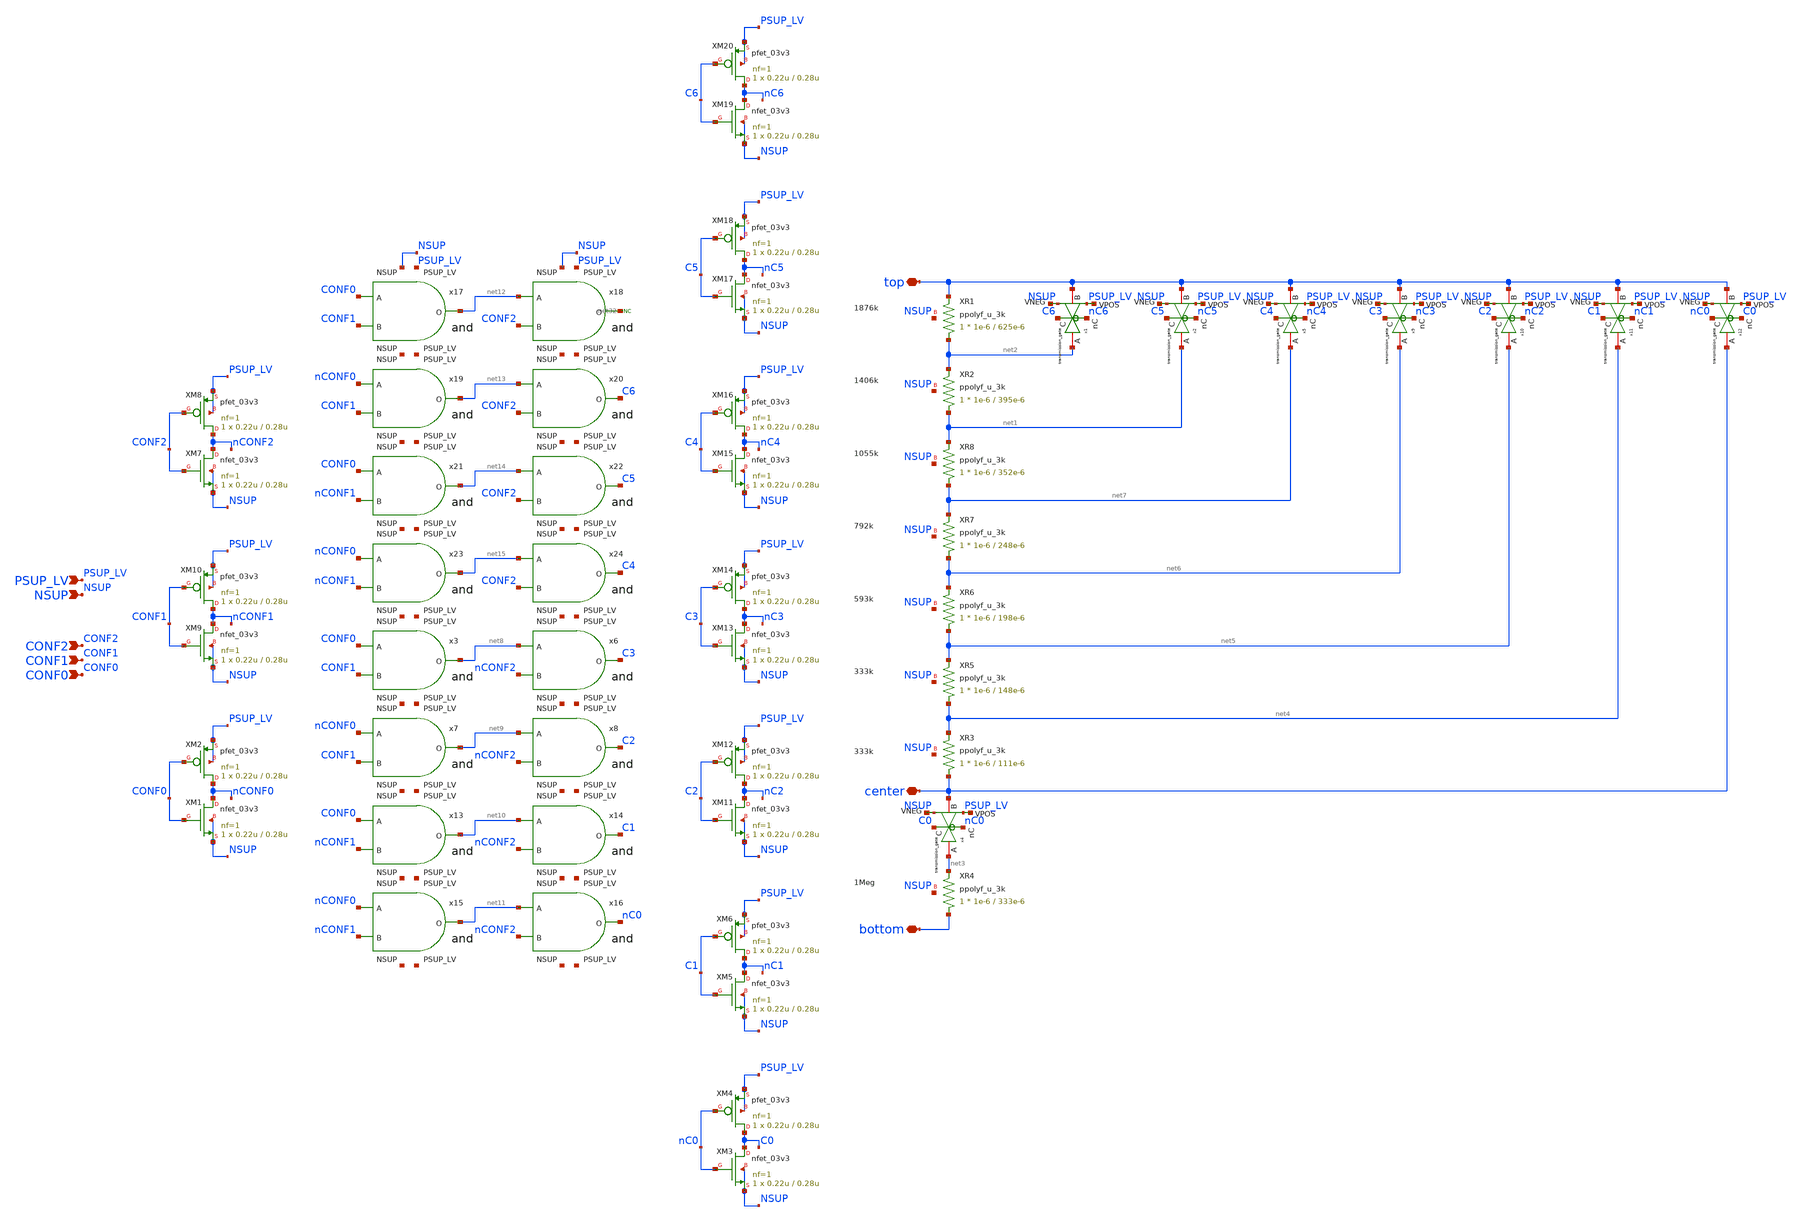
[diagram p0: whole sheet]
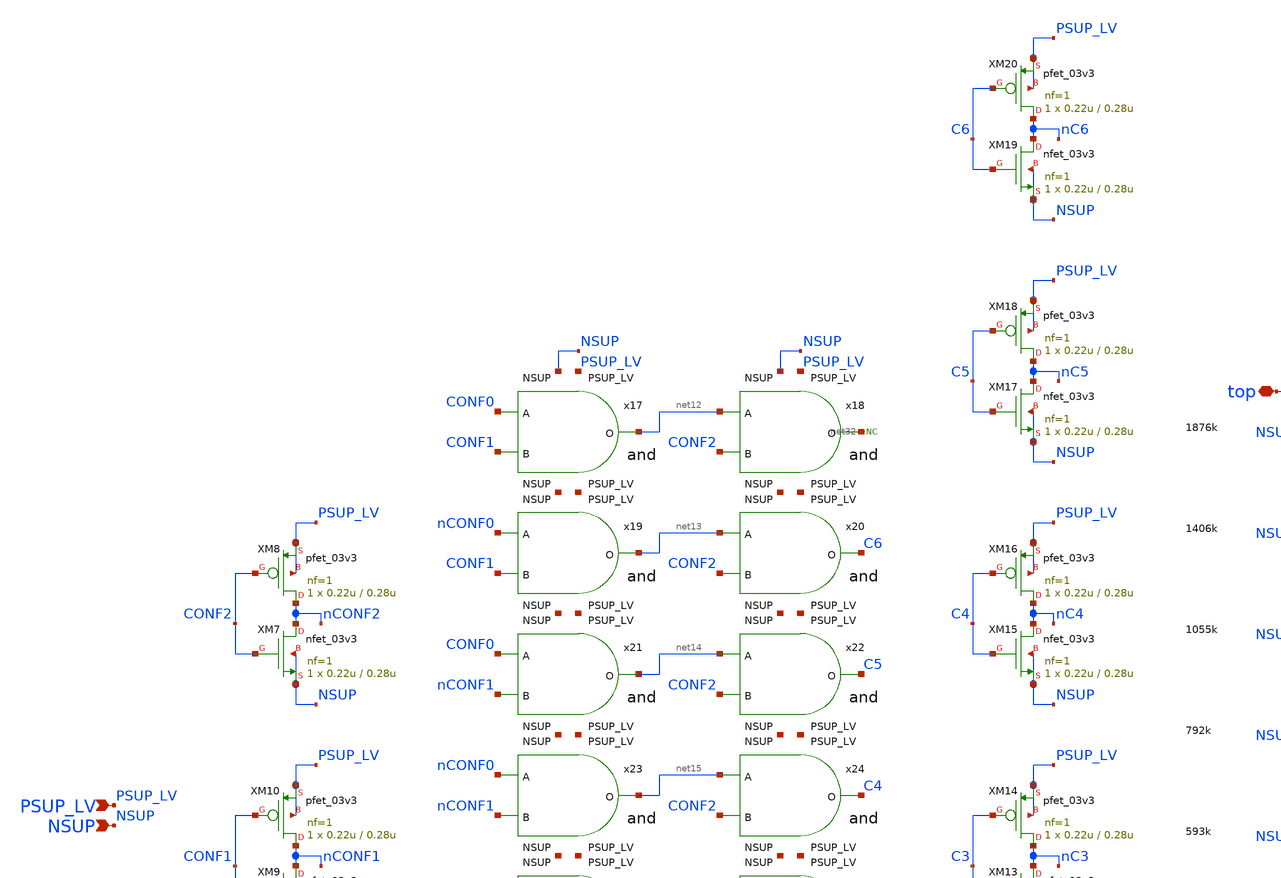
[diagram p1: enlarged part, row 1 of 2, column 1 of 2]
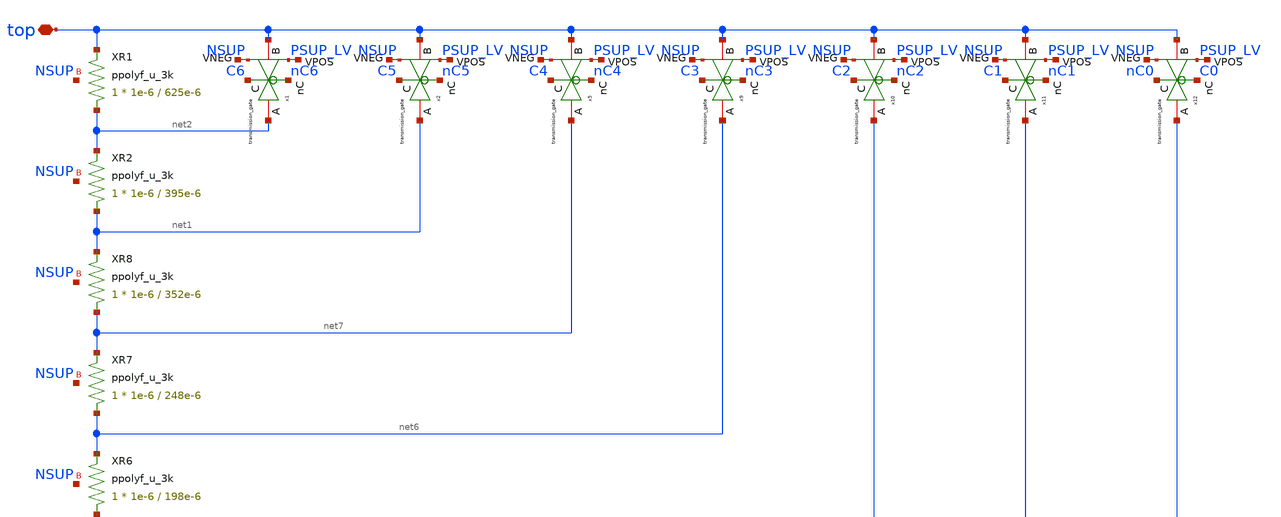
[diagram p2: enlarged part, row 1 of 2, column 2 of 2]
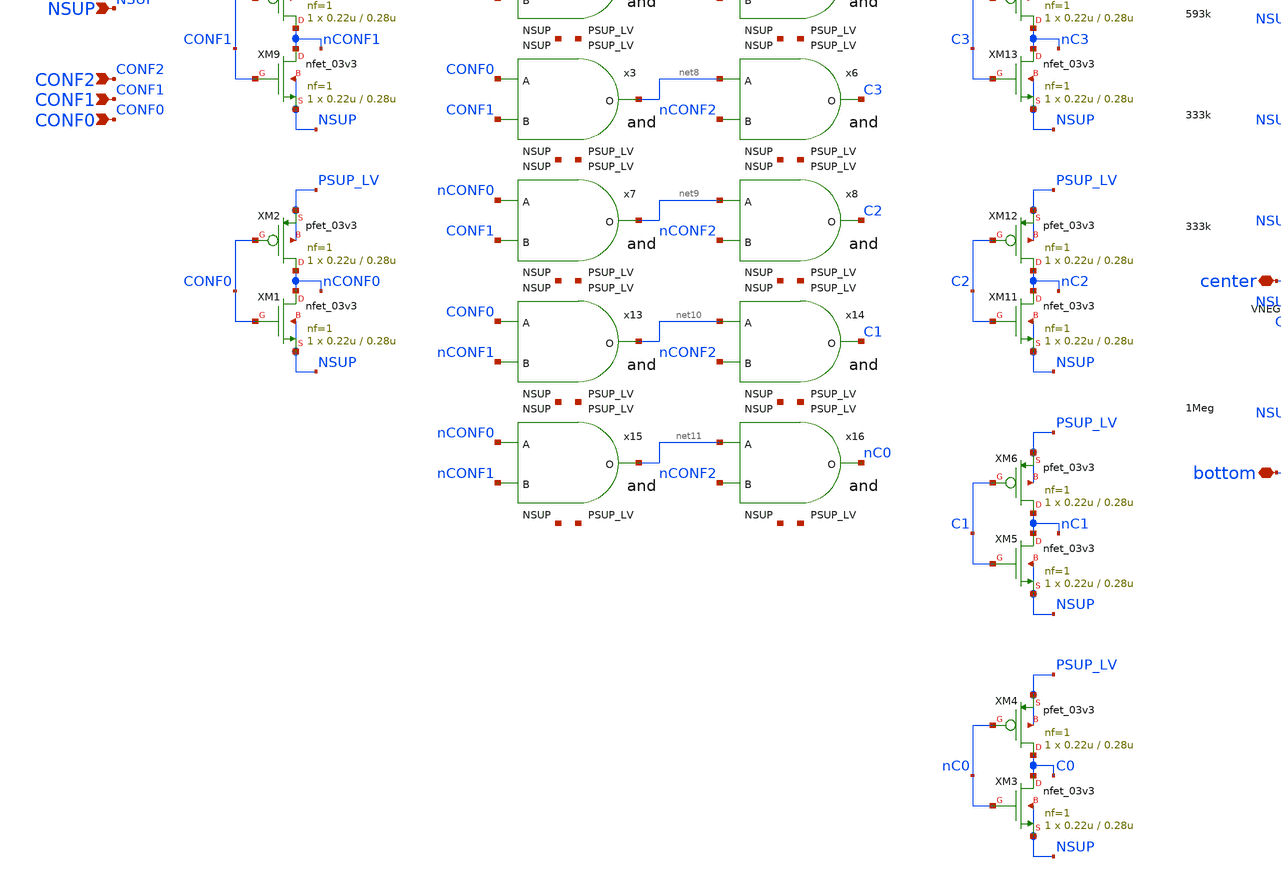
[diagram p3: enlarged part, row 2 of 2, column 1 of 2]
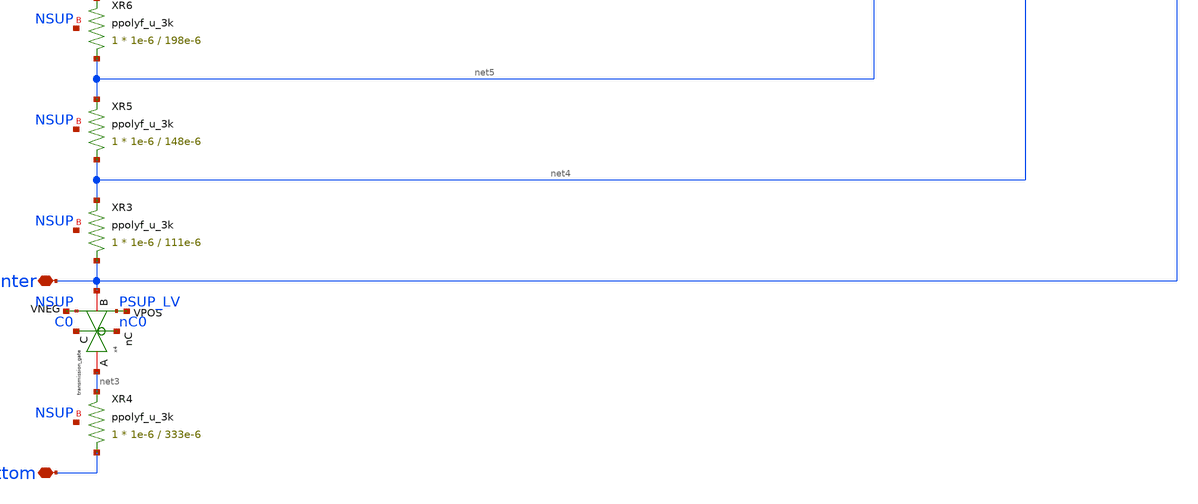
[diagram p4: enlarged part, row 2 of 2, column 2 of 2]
** sch_path: xschem/blocks/LPF_gain_fb/LPF_gain_fb.sch
**.subckt LPF_gain_fb top center bottom PSUP_LV NSUP CONF1 CONF2 CONF0
*.iopin top
*.iopin center
*.iopin bottom
*.ipin PSUP_LV
*.ipin NSUP
*.ipin CONF1
*.ipin CONF2
*.ipin CONF0
XR1 net2 top NSUP ppolyf_u_3k r_width=1e-6 r_length=625e-6 m=1
XR2 net1 net2 NSUP ppolyf_u_3k r_width=1e-6 r_length=395e-6 m=1
XR3 center net4 NSUP ppolyf_u_3k r_width=1e-6 r_length=111e-6 m=1
XR4 bottom net3 NSUP ppolyf_u_3k r_width=1e-6 r_length=333e-6 m=1
XM7 nCONF2 CONF2 NSUP NSUP nfet_03v3 L=0.28u W=0.22u nf=1 ad='int((nf+1)/2) * W/nf * 0.18u' as='int((nf+2)/2) * W/nf * 0.18u'
+ pd='2*int((nf+1)/2) * (W/nf + 0.18u)' ps='2*int((nf+2)/2) * (W/nf + 0.18u)' nrd='0.18u / W' nrs='0.18u / W'
+ sa=0 sb=0 sd=0 m=1
XM8 nCONF2 CONF2 PSUP_LV PSUP_LV pfet_03v3 L=0.28u W=0.22u nf=1 ad='int((nf+1)/2) * W/nf * 0.18u' as='int((nf+2)/2) * W/nf * 0.18u'
+ pd='2*int((nf+1)/2) * (W/nf + 0.18u)' ps='2*int((nf+2)/2) * (W/nf + 0.18u)' nrd='0.18u / W' nrs='0.18u / W'
+ sa=0 sb=0 sd=0 m=1
XM9 nCONF1 CONF1 NSUP NSUP nfet_03v3 L=0.28u W=0.22u nf=1 ad='int((nf+1)/2) * W/nf * 0.18u' as='int((nf+2)/2) * W/nf * 0.18u'
+ pd='2*int((nf+1)/2) * (W/nf + 0.18u)' ps='2*int((nf+2)/2) * (W/nf + 0.18u)' nrd='0.18u / W' nrs='0.18u / W'
+ sa=0 sb=0 sd=0 m=1
XM10 nCONF1 CONF1 PSUP_LV PSUP_LV pfet_03v3 L=0.28u W=0.22u nf=1 ad='int((nf+1)/2) * W/nf * 0.18u' as='int((nf+2)/2) * W/nf * 0.18u'
+ pd='2*int((nf+1)/2) * (W/nf + 0.18u)' ps='2*int((nf+2)/2) * (W/nf + 0.18u)' nrd='0.18u / W' nrs='0.18u / W'
+ sa=0 sb=0 sd=0 m=1
XM1 nCONF0 CONF0 NSUP NSUP nfet_03v3 L=0.28u W=0.22u nf=1 ad='int((nf+1)/2) * W/nf * 0.18u' as='int((nf+2)/2) * W/nf * 0.18u'
+ pd='2*int((nf+1)/2) * (W/nf + 0.18u)' ps='2*int((nf+2)/2) * (W/nf + 0.18u)' nrd='0.18u / W' nrs='0.18u / W'
+ sa=0 sb=0 sd=0 m=1
XM2 nCONF0 CONF0 PSUP_LV PSUP_LV pfet_03v3 L=0.28u W=0.22u nf=1 ad='int((nf+1)/2) * W/nf * 0.18u' as='int((nf+2)/2) * W/nf * 0.18u'
+ pd='2*int((nf+1)/2) * (W/nf + 0.18u)' ps='2*int((nf+2)/2) * (W/nf + 0.18u)' nrd='0.18u / W' nrs='0.18u / W'
+ sa=0 sb=0 sd=0 m=1
XM3 C0 nC0 NSUP NSUP nfet_03v3 L=0.28u W=0.22u nf=1 ad='int((nf+1)/2) * W/nf * 0.18u' as='int((nf+2)/2) * W/nf * 0.18u'
+ pd='2*int((nf+1)/2) * (W/nf + 0.18u)' ps='2*int((nf+2)/2) * (W/nf + 0.18u)' nrd='0.18u / W' nrs='0.18u / W'
+ sa=0 sb=0 sd=0 m=1
XM4 C0 nC0 PSUP_LV PSUP_LV pfet_03v3 L=0.28u W=0.22u nf=1 ad='int((nf+1)/2) * W/nf * 0.18u' as='int((nf+2)/2) * W/nf * 0.18u'
+ pd='2*int((nf+1)/2) * (W/nf + 0.18u)' ps='2*int((nf+2)/2) * (W/nf + 0.18u)' nrd='0.18u / W' nrs='0.18u / W'
+ sa=0 sb=0 sd=0 m=1
XM5 nC1 C1 NSUP NSUP nfet_03v3 L=0.28u W=0.22u nf=1 ad='int((nf+1)/2) * W/nf * 0.18u' as='int((nf+2)/2) * W/nf * 0.18u'
+ pd='2*int((nf+1)/2) * (W/nf + 0.18u)' ps='2*int((nf+2)/2) * (W/nf + 0.18u)' nrd='0.18u / W' nrs='0.18u / W'
+ sa=0 sb=0 sd=0 m=1
XM6 nC1 C1 PSUP_LV PSUP_LV pfet_03v3 L=0.28u W=0.22u nf=1 ad='int((nf+1)/2) * W/nf * 0.18u' as='int((nf+2)/2) * W/nf * 0.18u'
+ pd='2*int((nf+1)/2) * (W/nf + 0.18u)' ps='2*int((nf+2)/2) * (W/nf + 0.18u)' nrd='0.18u / W' nrs='0.18u / W'
+ sa=0 sb=0 sd=0 m=1
XM11 nC2 C2 NSUP NSUP nfet_03v3 L=0.28u W=0.22u nf=1 ad='int((nf+1)/2) * W/nf * 0.18u' as='int((nf+2)/2) * W/nf * 0.18u'
+ pd='2*int((nf+1)/2) * (W/nf + 0.18u)' ps='2*int((nf+2)/2) * (W/nf + 0.18u)' nrd='0.18u / W' nrs='0.18u / W'
+ sa=0 sb=0 sd=0 m=1
XM12 nC2 C2 PSUP_LV PSUP_LV pfet_03v3 L=0.28u W=0.22u nf=1 ad='int((nf+1)/2) * W/nf * 0.18u' as='int((nf+2)/2) * W/nf * 0.18u'
+ pd='2*int((nf+1)/2) * (W/nf + 0.18u)' ps='2*int((nf+2)/2) * (W/nf + 0.18u)' nrd='0.18u / W' nrs='0.18u / W'
+ sa=0 sb=0 sd=0 m=1
XM13 nC3 C3 NSUP NSUP nfet_03v3 L=0.28u W=0.22u nf=1 ad='int((nf+1)/2) * W/nf * 0.18u' as='int((nf+2)/2) * W/nf * 0.18u'
+ pd='2*int((nf+1)/2) * (W/nf + 0.18u)' ps='2*int((nf+2)/2) * (W/nf + 0.18u)' nrd='0.18u / W' nrs='0.18u / W'
+ sa=0 sb=0 sd=0 m=1
XM14 nC3 C3 PSUP_LV PSUP_LV pfet_03v3 L=0.28u W=0.22u nf=1 ad='int((nf+1)/2) * W/nf * 0.18u' as='int((nf+2)/2) * W/nf * 0.18u'
+ pd='2*int((nf+1)/2) * (W/nf + 0.18u)' ps='2*int((nf+2)/2) * (W/nf + 0.18u)' nrd='0.18u / W' nrs='0.18u / W'
+ sa=0 sb=0 sd=0 m=1
x4 C0 net3 center nC0 net16 net17 transmission_gate
x1 C6 net2 top nC6 net18 net19 transmission_gate
x2 C5 net1 top nC5 net20 net21 transmission_gate
XR5 net4 net5 NSUP ppolyf_u_3k r_width=1e-6 r_length=148e-6 m=1
XR6 net5 net6 NSUP ppolyf_u_3k r_width=1e-6 r_length=198e-6 m=1
XR7 net6 net7 NSUP ppolyf_u_3k r_width=1e-6 r_length=248e-6 m=1
XR8 net7 net1 NSUP ppolyf_u_3k r_width=1e-6 r_length=352e-6 m=1
x5 C4 net7 top nC4 net22 net23 transmission_gate
x9 C3 net6 top nC3 net24 net25 transmission_gate
x10 C2 net5 top nC2 net26 net27 transmission_gate
x11 C1 net4 top nC1 net28 net29 transmission_gate
XM15 nC4 C4 NSUP NSUP nfet_03v3 L=0.28u W=0.22u nf=1 ad='int((nf+1)/2) * W/nf * 0.18u' as='int((nf+2)/2) * W/nf * 0.18u'
+ pd='2*int((nf+1)/2) * (W/nf + 0.18u)' ps='2*int((nf+2)/2) * (W/nf + 0.18u)' nrd='0.18u / W' nrs='0.18u / W'
+ sa=0 sb=0 sd=0 m=1
XM16 nC4 C4 PSUP_LV PSUP_LV pfet_03v3 L=0.28u W=0.22u nf=1 ad='int((nf+1)/2) * W/nf * 0.18u' as='int((nf+2)/2) * W/nf * 0.18u'
+ pd='2*int((nf+1)/2) * (W/nf + 0.18u)' ps='2*int((nf+2)/2) * (W/nf + 0.18u)' nrd='0.18u / W' nrs='0.18u / W'
+ sa=0 sb=0 sd=0 m=1
XM17 nC5 C5 NSUP NSUP nfet_03v3 L=0.28u W=0.22u nf=1 ad='int((nf+1)/2) * W/nf * 0.18u' as='int((nf+2)/2) * W/nf * 0.18u'
+ pd='2*int((nf+1)/2) * (W/nf + 0.18u)' ps='2*int((nf+2)/2) * (W/nf + 0.18u)' nrd='0.18u / W' nrs='0.18u / W'
+ sa=0 sb=0 sd=0 m=1
XM18 nC5 C5 PSUP_LV PSUP_LV pfet_03v3 L=0.28u W=0.22u nf=1 ad='int((nf+1)/2) * W/nf * 0.18u' as='int((nf+2)/2) * W/nf * 0.18u'
+ pd='2*int((nf+1)/2) * (W/nf + 0.18u)' ps='2*int((nf+2)/2) * (W/nf + 0.18u)' nrd='0.18u / W' nrs='0.18u / W'
+ sa=0 sb=0 sd=0 m=1
XM19 nC6 C6 NSUP NSUP nfet_03v3 L=0.28u W=0.22u nf=1 ad='int((nf+1)/2) * W/nf * 0.18u' as='int((nf+2)/2) * W/nf * 0.18u'
+ pd='2*int((nf+1)/2) * (W/nf + 0.18u)' ps='2*int((nf+2)/2) * (W/nf + 0.18u)' nrd='0.18u / W' nrs='0.18u / W'
+ sa=0 sb=0 sd=0 m=1
XM20 nC6 C6 PSUP_LV PSUP_LV pfet_03v3 L=0.28u W=0.22u nf=1 ad='int((nf+1)/2) * W/nf * 0.18u' as='int((nf+2)/2) * W/nf * 0.18u'
+ pd='2*int((nf+1)/2) * (W/nf + 0.18u)' ps='2*int((nf+2)/2) * (W/nf + 0.18u)' nrd='0.18u / W' nrs='0.18u / W'
+ sa=0 sb=0 sd=0 m=1
x12 nC0 center top C0 net30 net31 transmission_gate
x3 net8 CONF0 CONF1 PSUP_LV NSUP and
x6 C3 net8 nCONF2 PSUP_LV NSUP and
x7 net9 nCONF0 CONF1 PSUP_LV NSUP and
x8 C2 net9 nCONF2 PSUP_LV NSUP and
x13 net10 CONF0 nCONF1 PSUP_LV NSUP and
x14 C1 net10 nCONF2 PSUP_LV NSUP and
x15 net11 nCONF0 nCONF1 PSUP_LV NSUP and
x16 nC0 net11 nCONF2 PSUP_LV NSUP and
x17 net12 CONF0 CONF1 PSUP_LV NSUP and
x18 net32 net12 CONF2 PSUP_LV NSUP and
x19 net13 nCONF0 CONF1 PSUP_LV NSUP and
x20 C6 net13 CONF2 PSUP_LV NSUP and
x21 net14 CONF0 nCONF1 PSUP_LV NSUP and
x22 C5 net14 CONF2 PSUP_LV NSUP and
x23 net15 nCONF0 nCONF1 PSUP_LV NSUP and
x24 C4 net15 CONF2 PSUP_LV NSUP and
* noconn #net32
**.ends

* expanding   symbol:  blocks/transmission_gate/transmission_gate.sym # of pins=6
** sym_path: xschem/blocks/transmission_gate/transmission_gate.sym
** sch_path: xschem/blocks/transmission_gate/transmission_gate.sch
.subckt transmission_gate C A B nC VPOS VNEG
*.iopin A
*.iopin B
*.ipin C
*.ipin nC
*.ipin VPOS
*.ipin VNEG
XM3 A C B VNEG nfet_03v3 L=0.28u W=1u nf=1 ad='int((nf+1)/2) * W/nf * 0.18u' as='int((nf+2)/2) * W/nf * 0.18u'
+ pd='2*int((nf+1)/2) * (W/nf + 0.18u)' ps='2*int((nf+2)/2) * (W/nf + 0.18u)' nrd='0.18u / W' nrs='0.18u / W'
+ sa=0 sb=0 sd=0 m=1
XM4 A nC B VPOS pfet_03v3 L=0.28u W=1u nf=1 ad='int((nf+1)/2) * W/nf * 0.18u' as='int((nf+2)/2) * W/nf * 0.18u'
+ pd='2*int((nf+1)/2) * (W/nf + 0.18u)' ps='2*int((nf+2)/2) * (W/nf + 0.18u)' nrd='0.18u / W' nrs='0.18u / W'
+ sa=0 sb=0 sd=0 m=1
.ends


* expanding   symbol:  blocks/and/and.sym # of pins=7
** sym_path: xschem/blocks/and/and.sym
** sch_path: xschem/blocks/and/and.sch
.subckt and O A B PSUP_LV NSUP
*.ipin PSUP_LV
*.ipin NSUP
*.ipin A
*.ipin B
*.opin O
XM5 net1 B NSUP NSUP nfet_03v3 L=0.28u W=0.22u nf=1 ad='int((nf+1)/2) * W/nf * 0.18u' as='int((nf+2)/2) * W/nf * 0.18u'
+ pd='2*int((nf+1)/2) * (W/nf + 0.18u)' ps='2*int((nf+2)/2) * (W/nf + 0.18u)' nrd='0.18u / W' nrs='0.18u / W'
+ sa=0 sb=0 sd=0 m=1
XM1 net2 A net1 NSUP nfet_03v3 L=0.28u W=0.22u nf=1 ad='int((nf+1)/2) * W/nf * 0.18u' as='int((nf+2)/2) * W/nf * 0.18u'
+ pd='2*int((nf+1)/2) * (W/nf + 0.18u)' ps='2*int((nf+2)/2) * (W/nf + 0.18u)' nrd='0.18u / W' nrs='0.18u / W'
+ sa=0 sb=0 sd=0 m=1
XM2 net2 A PSUP_LV PSUP_LV pfet_03v3 L=0.28u W=0.22u nf=1 ad='int((nf+1)/2) * W/nf * 0.18u' as='int((nf+2)/2) * W/nf * 0.18u'
+ pd='2*int((nf+1)/2) * (W/nf + 0.18u)' ps='2*int((nf+2)/2) * (W/nf + 0.18u)' nrd='0.18u / W' nrs='0.18u / W'
+ sa=0 sb=0 sd=0 m=1
XM3 net2 B PSUP_LV PSUP_LV pfet_03v3 L=0.28u W=0.22u nf=1 ad='int((nf+1)/2) * W/nf * 0.18u' as='int((nf+2)/2) * W/nf * 0.18u'
+ pd='2*int((nf+1)/2) * (W/nf + 0.18u)' ps='2*int((nf+2)/2) * (W/nf + 0.18u)' nrd='0.18u / W' nrs='0.18u / W'
+ sa=0 sb=0 sd=0 m=1
XM4 O net2 PSUP_LV PSUP_LV pfet_03v3 L=0.28u W=0.22u nf=1 ad='int((nf+1)/2) * W/nf * 0.18u' as='int((nf+2)/2) * W/nf * 0.18u'
+ pd='2*int((nf+1)/2) * (W/nf + 0.18u)' ps='2*int((nf+2)/2) * (W/nf + 0.18u)' nrd='0.18u / W' nrs='0.18u / W'
+ sa=0 sb=0 sd=0 m=1
XM6 O net2 NSUP NSUP nfet_03v3 L=0.28u W=0.22u nf=1 ad='int((nf+1)/2) * W/nf * 0.18u' as='int((nf+2)/2) * W/nf * 0.18u'
+ pd='2*int((nf+1)/2) * (W/nf + 0.18u)' ps='2*int((nf+2)/2) * (W/nf + 0.18u)' nrd='0.18u / W' nrs='0.18u / W'
+ sa=0 sb=0 sd=0 m=1
.ends

.end
